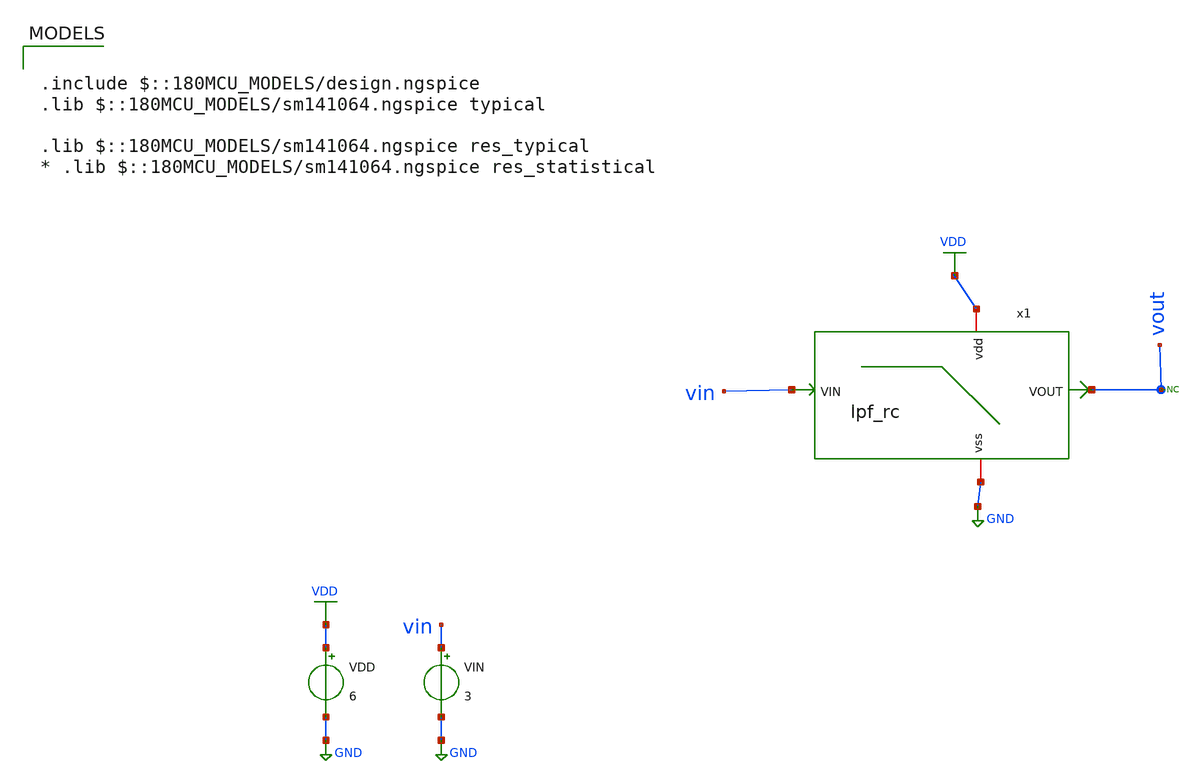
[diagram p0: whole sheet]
** sch_path: analog-db/circuits/ldo_005_buffered_ref/reference/ti-ldo/lpf/lpf_tb_ac.sch
**.subckt lpf_tb_ac
x1 net1 GND vout vin lpf_rc
VDD VDD GND 6
VIN vin GND 3
* noconn vout
**** begin user architecture code

.include $::180MCU_MODELS/design.ngspice
.lib $::180MCU_MODELS/sm141064.ngspice typical

.lib $::180MCU_MODELS/sm141064.ngspice res_typical
* .lib $::180MCU_MODELS/sm141064.ngspice res_statistical



* ====== NGSPICE_AC_Response Control Block ======
.control
save all

* === Sweep Params ===
let f_start = 1
let f_stop  = 1e9
let f_step  = 10

* === Source Setup ===
let vin_ac_mag = 1
let vin_dc_bias = 3.0
alter @VIN[DC] = $&vin_dc_bias
alter @VIN[AC] = $&vin_ac_mag

* === OP + AC Sweep ===
op
ac dec $&f_step $&f_start $&f_stop

* === Signal Processing ===
let vout_mag = abs(v(vout))
let vout_dB  = 20*log10(vout_mag)
*let vout_ph  = phase(v(vout))
let vout_ph  = 180/PI*cph(vout)


* === Plots ===
settype decibel out
plot vout_dB vs frequency xlimit $&f_start $&f_stop ylabel 'signal gain'

plot vout_ph vs frequency

* === Measurements ===
* Max Gain
meas ac gain_max max vout_dB
meas ac f_peak when vout_dB=GAIN_MAX

* 3dB below peak gain
let gain_3dB = gain_max - 3

* Lower and Upper 3dB Frequencies
*meas ac f_lo when vout_dB=gain_3dB fall=1
*meas ac f_hi when vout_dB=gain_3dB rise=1

* Post-Processing for BW and Q (use let)
* If previous failed, fallback values will be undefined or skipped
*let bw = f_hi - f_lo
*let q  = f_peak / bw

* Print Results
*print gain_max
*print f_peak
*print f_lo
*print f_hi
*print bw
*print q

* Save Raw
write NGSPICE_AC_Response.raw
.endc




**** end user architecture code
**.ends
.GLOBAL VDD
.GLOBAL GND
.end
